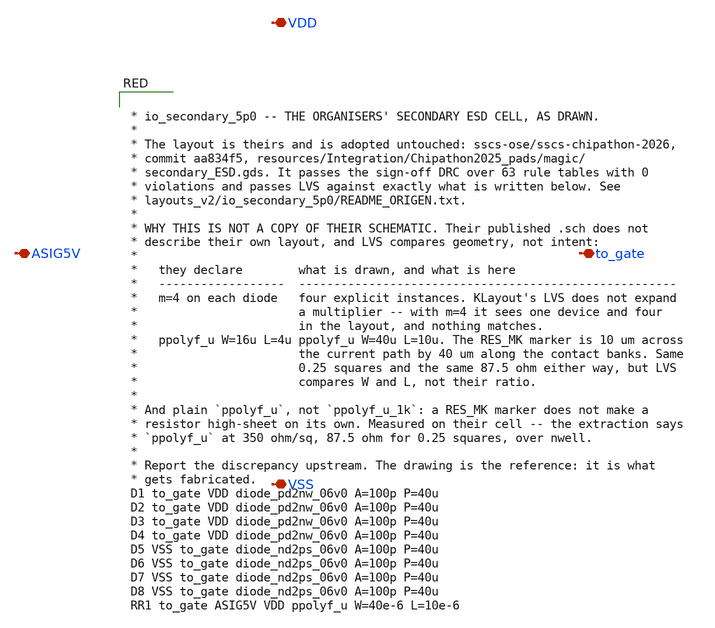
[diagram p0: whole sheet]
** sch_path: FINAL/XSCHEM_v2/io_secondary_5p0.sch
**.subckt io_secondary_5p0 VDD to_gate ASIG5V VSS
*.iopin VDD
*.iopin to_gate
*.iopin ASIG5V
*.iopin VSS
**** begin user architecture code


* io_secondary_5p0 -- THE ORGANISERS' SECONDARY ESD CELL, AS DRAWN.
*
* The layout is theirs and is adopted untouched: sscs-ose/sscs-chipathon-2026,
* commit aa834f5, resources/Integration/Chipathon2025_pads/magic/
* secondary_ESD.gds. It passes the sign-off DRC over 63 rule tables with 0
* violations and passes LVS against exactly what is written below. See
* layouts_v2/io_secondary_5p0/README_ORIGEN.txt.
*
* WHY THIS IS NOT A COPY OF THEIR SCHEMATIC. Their published .sch does not
* describe their own layout, and LVS compares geometry, not intent:
*
*   they declare        what is drawn, and what is here
*   ------------------  ------------------------------------------------------
*   m=4 on each diode   four explicit instances. KLayout's LVS does not expand
*                       a multiplier -- with m=4 it sees one device and four
*                       in the layout, and nothing matches.
*   ppolyf_u W=16u L=4u ppolyf_u W=40u L=10u. The RES_MK marker is 10 um across
*                       the current path by 40 um along the contact banks. Same
*                       0.25 squares and the same 87.5 ohm either way, but LVS
*                       compares W and L, not their ratio.
*
* And plain `ppolyf_u`, not `ppolyf_u_1k`: a RES_MK marker does not make a
* resistor high-sheet on its own. Measured on their cell -- the extraction says
* `ppolyf_u` at 350 ohm/sq, 87.5 ohm for 0.25 squares, over nwell.
*
* Report the discrepancy upstream. The drawing is the reference: it is what
* gets fabricated.
D1 to_gate VDD diode_pd2nw_06v0 A=100p P=40u
D2 to_gate VDD diode_pd2nw_06v0 A=100p P=40u
D3 to_gate VDD diode_pd2nw_06v0 A=100p P=40u
D4 to_gate VDD diode_pd2nw_06v0 A=100p P=40u
D5 VSS to_gate diode_nd2ps_06v0 A=100p P=40u
D6 VSS to_gate diode_nd2ps_06v0 A=100p P=40u
D7 VSS to_gate diode_nd2ps_06v0 A=100p P=40u
D8 VSS to_gate diode_nd2ps_06v0 A=100p P=40u
RR1 to_gate ASIG5V VDD ppolyf_u W=40e-6 L=10e-6


**** end user architecture code
**.ends
.end
